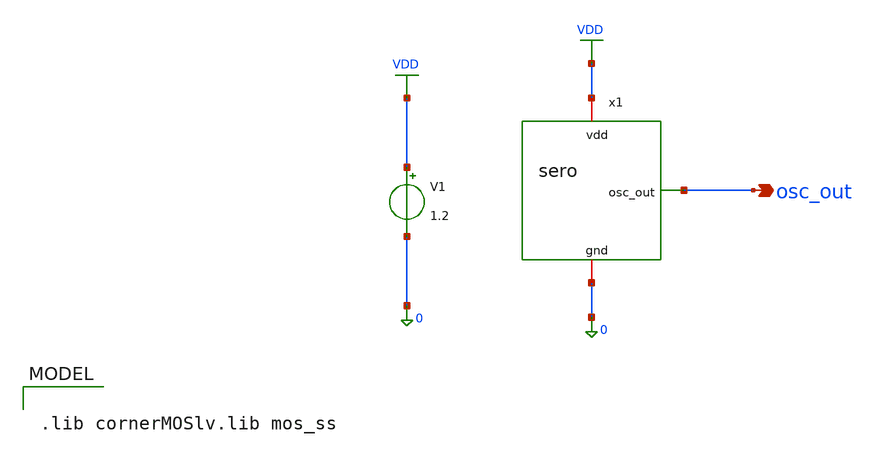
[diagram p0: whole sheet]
** sch_path: simulations/tb/freq_v_length.sch
**.subckt freq_v_length osc_out
*.opin osc_out
x1 VDD osc_out 0 sero
V1 VDD 0 1.2
**** begin user architecture code

.lib cornerMOSlv.lib mos_ss



.param length=0.13u
.control
  save all
  let l_start = 0.13e-6
  let l_stop  = 0.40e-6
  let l_step  = 0.03e-6
  let n_pts   = 10
  let lengths = vector(n_pts)
  let freqs   = vector(n_pts)
  let idx = 0

  while idx < n_pts
    let l_curr = l_start + idx * l_step
    alterparam length = $&l_curr
    reset

    let tstop_val = 8e-9 * (l_curr / 0.13e-6)
    tran 1p $&tstop_val uic

    meas tran t1 when v(osc_out)=0.6 rise=4
    meas tran t2 when v(osc_out)=0.6 rise=5

    let freqs[idx]   = 1 / (t2 - t1)
    let lengths[idx] = l_curr

    let idx = idx + 1
  end

  set curplot = control
  write freq_v_length.raw freqs lengths
.endc


**** end user architecture code
**.ends
.GLOBAL VDD
.end
